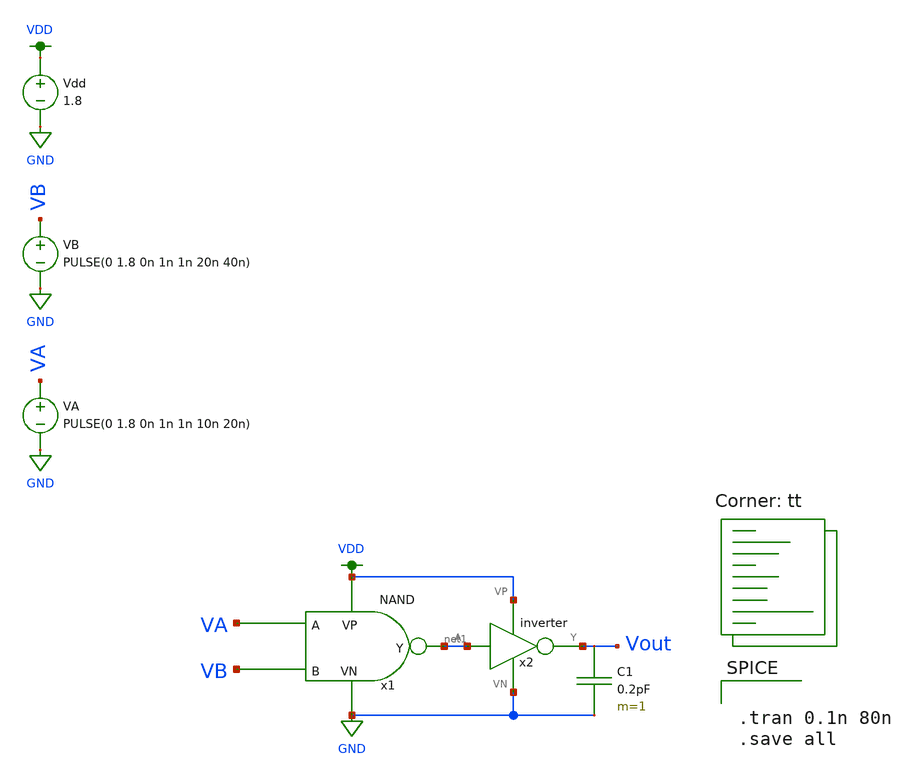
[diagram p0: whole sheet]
** sch_path: MADVLSI_MP1/AND(NANDINV).sch
**.subckt AND(NANDINV)
VB VB GND PULSE(0 1.8 0n 1n 1n 20n 40n)
VA VA GND PULSE(0 1.8 0n 1n 1n 10n 20n)
Vdd VDD GND 1.8
C1 Vout GND 0.2pF m=1
x1 VDD VA VB net1 GND NAND
x2 VDD net1 Vout GND inverter
**** begin user architecture code


.tran 0.1n 80n
.save all

.lib $::SKYWATER_MODELS/sky130.lib.spice tt
**** end user architecture code
**.ends

* expanding   symbol:  /home/allan/Documents/MADVLSI_Projects/MADVLSI_MP1/NAND.sym # of pins=5
** sym_path: MADVLSI_MP1/NAND.sym
** sch_path: MADVLSI_MP1/NAND.sch
.subckt NAND VP A B Y VN
*.ipin A
*.ipin B
*.iopin VP
*.iopin VN
*.opin Y
XM1 Y A VP VP sky130_fd_pr__pfet_01v8 L=0.15 W=1 nf=1 ad='int((nf+1)/2) * W/nf * 0.29' as='int((nf+2)/2) * W/nf * 0.29'
+ pd='2*int((nf+1)/2) * (W/nf + 0.29)' ps='2*int((nf+2)/2) * (W/nf + 0.29)' nrd='0.29 / W' nrs='0.29 / W'
+ sa=0 sb=0 sd=0 mult=1 m=1
XM2 VP B Y VP sky130_fd_pr__pfet_01v8 L=0.15 W=1 nf=1 ad='int((nf+1)/2) * W/nf * 0.29' as='int((nf+2)/2) * W/nf * 0.29'
+ pd='2*int((nf+1)/2) * (W/nf + 0.29)' ps='2*int((nf+2)/2) * (W/nf + 0.29)' nrd='0.29 / W' nrs='0.29 / W'
+ sa=0 sb=0 sd=0 mult=1 m=1
XM3 Y A net1 VN sky130_fd_pr__nfet_01v8 L=0.15 W=1 nf=1 ad='int((nf+1)/2) * W/nf * 0.29' as='int((nf+2)/2) * W/nf * 0.29'
+ pd='2*int((nf+1)/2) * (W/nf + 0.29)' ps='2*int((nf+2)/2) * (W/nf + 0.29)' nrd='0.29 / W' nrs='0.29 / W'
+ sa=0 sb=0 sd=0 mult=1 m=1
XM4 net1 B VN VN sky130_fd_pr__nfet_01v8 L=0.15 W=1 nf=1 ad='int((nf+1)/2) * W/nf * 0.29' as='int((nf+2)/2) * W/nf * 0.29'
+ pd='2*int((nf+1)/2) * (W/nf + 0.29)' ps='2*int((nf+2)/2) * (W/nf + 0.29)' nrd='0.29 / W' nrs='0.29 / W'
+ sa=0 sb=0 sd=0 mult=1 m=1
.ends


* expanding   symbol:  /home/allan/Documents/MADVLSI_Projects/MADVLSI_MP1/inverter.sym # of pins=4
** sym_path: MADVLSI_MP1/inverter.sym
** sch_path: MADVLSI_MP1/inverter.sch
.subckt inverter VP A Y VN
*.ipin A
*.iopin VP
*.iopin VN
*.opin Y
XM1 Y A VN VN sky130_fd_pr__nfet_01v8 L=0.15 W=1 nf=1 ad='int((nf+1)/2) * W/nf * 0.29' as='int((nf+2)/2) * W/nf * 0.29'
+ pd='2*int((nf+1)/2) * (W/nf + 0.29)' ps='2*int((nf+2)/2) * (W/nf + 0.29)' nrd='0.29 / W' nrs='0.29 / W'
+ sa=0 sb=0 sd=0 mult=1 m=1
XM2 Y A VP VP sky130_fd_pr__pfet_01v8 L=0.15 W=1 nf=1 ad='int((nf+1)/2) * W/nf * 0.29' as='int((nf+2)/2) * W/nf * 0.29'
+ pd='2*int((nf+1)/2) * (W/nf + 0.29)' ps='2*int((nf+2)/2) * (W/nf + 0.29)' nrd='0.29 / W' nrs='0.29 / W'
+ sa=0 sb=0 sd=0 mult=1 m=1
.ends

.GLOBAL GND
.GLOBAL VDD
.end
